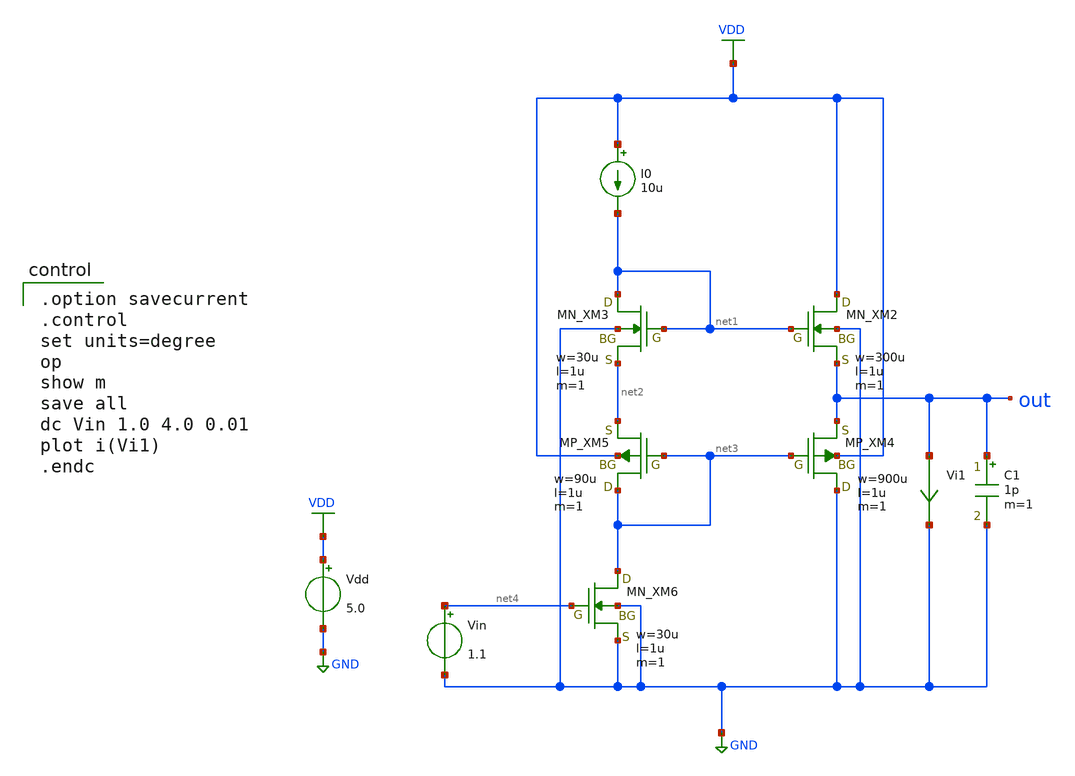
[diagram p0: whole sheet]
** sch_path: schematic/20250924_OSS_Workshop/ishikai/buf_pushpull/buf_pushpull_tb.sch
**.subckt buf_pushpull_tb
Vdd VDD GND 5.0
I0 VDD net1 10u
Vi1 out GND 0
.save i(vi1)
Vin net4 GND 1.1
C1 out GND 1p m=1
XM3 net1 net1 net2 GND NMOS w=30u l=1u as=0 ad=0 ps=0 pd=0 nrd=0 nrs=0 m=1
XM2 VDD net1 out GND NMOS w=300u l=1u as=0 ad=0 ps=0 pd=0 nrd=0 nrs=0 m=1
XM5 net3 net3 net2 VDD PMOS w=90u l=1u as=0 ad=0 ps=0 pd=0 nrd=0 nrs=0 m=1
XM4 GND net3 out VDD PMOS w=900u l=1u as=0 ad=0 ps=0 pd=0 nrd=0 nrs=0 m=1
XM6 net3 net4 GND GND NMOS w=30u l=1u as=0 ad=0 ps=0 pd=0 nrd=0 nrs=0 m=1
**** begin user architecture code

.option savecurrent
.control
set units=degree
op
show m
save all
dc Vin 1.0 4.0 0.01
plot i(Vi1)
.endc

 .include $::LIB/../ip62_models
**** end user architecture code
**.ends
.GLOBAL GND
.GLOBAL VDD
.end
